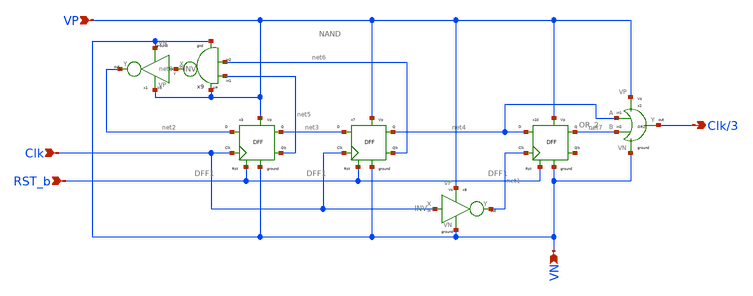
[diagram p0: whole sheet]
** sch_path: Blocks/Divide by 3 Circuit/div3.sch
**.subckt div3 Clk/3 Clk VN RST_b VP
*.opin Clk/3
*.ipin Clk
*.ipin VN
*.ipin RST_b
*.ipin VP
x3 net2 Clk RST_b VN VP net3 net5 DFF1
x8 Clk net1 VP VN INV
x1 net8 net2 VP VN INV
x9 net6 net5 net8 VP VN NAND
x2 net7 net4 Clk/3 VP VN OR_2
x7 net3 Clk RST_b VN VP net4 net6 DFF1
x10 net4 net1 RST_b VN VP net7 net9 DFF1
**.ends

* expanding   symbol:  pico_chipathon/component/FlipFlops/DFF1.sym # of pins=7
** sym_path: component/FlipFlops/DFF1.sym
** sch_path: component/FlipFlops/DFF1.sch
.subckt DFF1 D Clk RST VN VP Q Qb
*.opin Q
*.iopin VN
*.iopin VP
*.ipin Clk
*.ipin D
*.ipin RST
*.opin Qb
x7 net2 net4 net3 VP VN NAND
x8 net3 Clk RST VP VN net2 NAND3
x6 Q net1 RST VP VN Qb NAND3
x4 net2 Clk net4 VP VN net1 NAND3
x5 net1 D RST VP VN net4 NAND3
x1 Qb net2 Q VP VN NAND
.ends


* expanding   symbol:  pico_chipathon/component/INV/INV.sym # of pins=4
** sym_path: component/INV/INV.sym
** sch_path: component/INV/INV.sch
.subckt INV X Y VP VN
*.ipin X
*.opin Y
*.iopin VN
*.iopin VP
XM1 Y X VN VN sky130_fd_pr__nfet_01v8 L=0.15 W=0.42 nf=1 ad='int((nf+1)/2) * W/nf * 0.29' as='int((nf+2)/2) * W/nf * 0.29'
+ pd='2*int((nf+1)/2) * (W/nf + 0.29)' ps='2*int((nf+2)/2) * (W/nf + 0.29)' nrd='0.29 / W' nrs='0.29 / W'
+ sa=0 sb=0 sd=0 mult=1 m=1
XM2 Y X VP VP sky130_fd_pr__pfet_01v8 L=0.15 W=1.26 nf=1 ad='int((nf+1)/2) * W/nf * 0.29' as='int((nf+2)/2) * W/nf * 0.29'
+ pd='2*int((nf+1)/2) * (W/nf + 0.29)' ps='2*int((nf+2)/2) * (W/nf + 0.29)' nrd='0.29 / W' nrs='0.29 / W'
+ sa=0 sb=0 sd=0 mult=1 m=1
.ends


* expanding   symbol:  pico_chipathon/component/NAND2/NAND.sym # of pins=5
** sym_path: component/NAND2/NAND.sym
** sch_path: component/NAND2/NAND.sch
.subckt NAND B A Y VP VN
*.iopin VP
*.ipin A
*.ipin B
*.opin Y
*.iopin VN
XM1 Y A VP VP sky130_fd_pr__pfet_01v8 L=0.15 W=1.26 nf=1 ad='int((nf+1)/2) * W/nf * 0.29' as='int((nf+2)/2) * W/nf * 0.29'
+ pd='2*int((nf+1)/2) * (W/nf + 0.29)' ps='2*int((nf+2)/2) * (W/nf + 0.29)' nrd='0.29 / W' nrs='0.29 / W'
+ sa=0 sb=0 sd=0 mult=1 m=1
XM2 Y B VP VP sky130_fd_pr__pfet_01v8 L=0.15 W=1.26 nf=1 ad='int((nf+1)/2) * W/nf * 0.29' as='int((nf+2)/2) * W/nf * 0.29'
+ pd='2*int((nf+1)/2) * (W/nf + 0.29)' ps='2*int((nf+2)/2) * (W/nf + 0.29)' nrd='0.29 / W' nrs='0.29 / W'
+ sa=0 sb=0 sd=0 mult=1 m=1
XM3 Y A net1 net1 sky130_fd_pr__nfet_01v8 L=0.15 W=0.84 nf=1 ad='int((nf+1)/2) * W/nf * 0.29' as='int((nf+2)/2) * W/nf * 0.29'
+ pd='2*int((nf+1)/2) * (W/nf + 0.29)' ps='2*int((nf+2)/2) * (W/nf + 0.29)' nrd='0.29 / W' nrs='0.29 / W'
+ sa=0 sb=0 sd=0 mult=1 m=1
XM4 net1 B VN VN sky130_fd_pr__nfet_01v8 L=0.15 W=0.84 nf=1 ad='int((nf+1)/2) * W/nf * 0.29' as='int((nf+2)/2) * W/nf * 0.29'
+ pd='2*int((nf+1)/2) * (W/nf + 0.29)' ps='2*int((nf+2)/2) * (W/nf + 0.29)' nrd='0.29 / W' nrs='0.29 / W'
+ sa=0 sb=0 sd=0 mult=1 m=1
.ends


* expanding   symbol:  pico_chipathon/component/OR2/OR_2.sym # of pins=5
** sym_path: component/OR2/OR_2.sym
** sch_path: component/OR2/OR_2.sch
.subckt OR_2 B A Y VP VN
*.iopin VP
*.iopin VN
*.ipin A
*.ipin B
*.opin Y
XM1 net1 B VN VN sky130_fd_pr__nfet_01v8 L=0.15 W=0.42 nf=1 ad='int((nf+1)/2) * W/nf * 0.29' as='int((nf+2)/2) * W/nf * 0.29'
+ pd='2*int((nf+1)/2) * (W/nf + 0.29)' ps='2*int((nf+2)/2) * (W/nf + 0.29)' nrd='0.29 / W' nrs='0.29 / W'
+ sa=0 sb=0 sd=0 mult=1 m=1
XM2 net1 A VN VN sky130_fd_pr__nfet_01v8 L=0.15 W=0.42 nf=1 ad='int((nf+1)/2) * W/nf * 0.29' as='int((nf+2)/2) * W/nf * 0.29'
+ pd='2*int((nf+1)/2) * (W/nf + 0.29)' ps='2*int((nf+2)/2) * (W/nf + 0.29)' nrd='0.29 / W' nrs='0.29 / W'
+ sa=0 sb=0 sd=0 mult=1 m=1
XM3 net1 B net2 VP sky130_fd_pr__pfet_01v8 L=0.15 W=2.52 nf=1 ad='int((nf+1)/2) * W/nf * 0.29' as='int((nf+2)/2) * W/nf * 0.29'
+ pd='2*int((nf+1)/2) * (W/nf + 0.29)' ps='2*int((nf+2)/2) * (W/nf + 0.29)' nrd='0.29 / W' nrs='0.29 / W'
+ sa=0 sb=0 sd=0 mult=1 m=1
XM4 net2 A VP VP sky130_fd_pr__pfet_01v8 L=0.15 W=2.52 nf=1 ad='int((nf+1)/2) * W/nf * 0.29' as='int((nf+2)/2) * W/nf * 0.29'
+ pd='2*int((nf+1)/2) * (W/nf + 0.29)' ps='2*int((nf+2)/2) * (W/nf + 0.29)' nrd='0.29 / W' nrs='0.29 / W'
+ sa=0 sb=0 sd=0 mult=1 m=1
x1 net1 Y VP VN INV
.ends


* expanding   symbol:  component/NAND3/NAND3.sym # of pins=6
** sym_path: component/NAND3/NAND3.sym
** sch_path: component/NAND3/NAND3.sch
.subckt NAND3 A B C VP VN Y
*.iopin VP
*.iopin VN
*.ipin A
*.ipin B
*.ipin C
*.opin Y
XM1 Y A net1 VN sky130_fd_pr__nfet_01v8 L=0.15 W=1.26 nf=1 ad='int((nf+1)/2) * W/nf * 0.29' as='int((nf+2)/2) * W/nf * 0.29'
+ pd='2*int((nf+1)/2) * (W/nf + 0.29)' ps='2*int((nf+2)/2) * (W/nf + 0.29)' nrd='0.29 / W' nrs='0.29 / W'
+ sa=0 sb=0 sd=0 mult=1 m=1
XM2 net1 B net2 VN sky130_fd_pr__nfet_01v8 L=0.15 W=1.26 nf=1 ad='int((nf+1)/2) * W/nf * 0.29' as='int((nf+2)/2) * W/nf * 0.29'
+ pd='2*int((nf+1)/2) * (W/nf + 0.29)' ps='2*int((nf+2)/2) * (W/nf + 0.29)' nrd='0.29 / W' nrs='0.29 / W'
+ sa=0 sb=0 sd=0 mult=1 m=1
XM3 net2 C VN VN sky130_fd_pr__nfet_01v8 L=0.15 W=1.26 nf=1 ad='int((nf+1)/2) * W/nf * 0.29' as='int((nf+2)/2) * W/nf * 0.29'
+ pd='2*int((nf+1)/2) * (W/nf + 0.29)' ps='2*int((nf+2)/2) * (W/nf + 0.29)' nrd='0.29 / W' nrs='0.29 / W'
+ sa=0 sb=0 sd=0 mult=1 m=1
XM4 Y A VP VP sky130_fd_pr__pfet_01v8 L=0.15 W=1.26 nf=1 ad='int((nf+1)/2) * W/nf * 0.29' as='int((nf+2)/2) * W/nf * 0.29'
+ pd='2*int((nf+1)/2) * (W/nf + 0.29)' ps='2*int((nf+2)/2) * (W/nf + 0.29)' nrd='0.29 / W' nrs='0.29 / W'
+ sa=0 sb=0 sd=0 mult=1 m=1
XM5 Y B VP VP sky130_fd_pr__pfet_01v8 L=0.15 W=1.26 nf=1 ad='int((nf+1)/2) * W/nf * 0.29' as='int((nf+2)/2) * W/nf * 0.29'
+ pd='2*int((nf+1)/2) * (W/nf + 0.29)' ps='2*int((nf+2)/2) * (W/nf + 0.29)' nrd='0.29 / W' nrs='0.29 / W'
+ sa=0 sb=0 sd=0 mult=1 m=1
XM6 Y C VP VP sky130_fd_pr__pfet_01v8 L=0.15 W=1.26 nf=1 ad='int((nf+1)/2) * W/nf * 0.29' as='int((nf+2)/2) * W/nf * 0.29'
+ pd='2*int((nf+1)/2) * (W/nf + 0.29)' ps='2*int((nf+2)/2) * (W/nf + 0.29)' nrd='0.29 / W' nrs='0.29 / W'
+ sa=0 sb=0 sd=0 mult=1 m=1
.ends

.end
